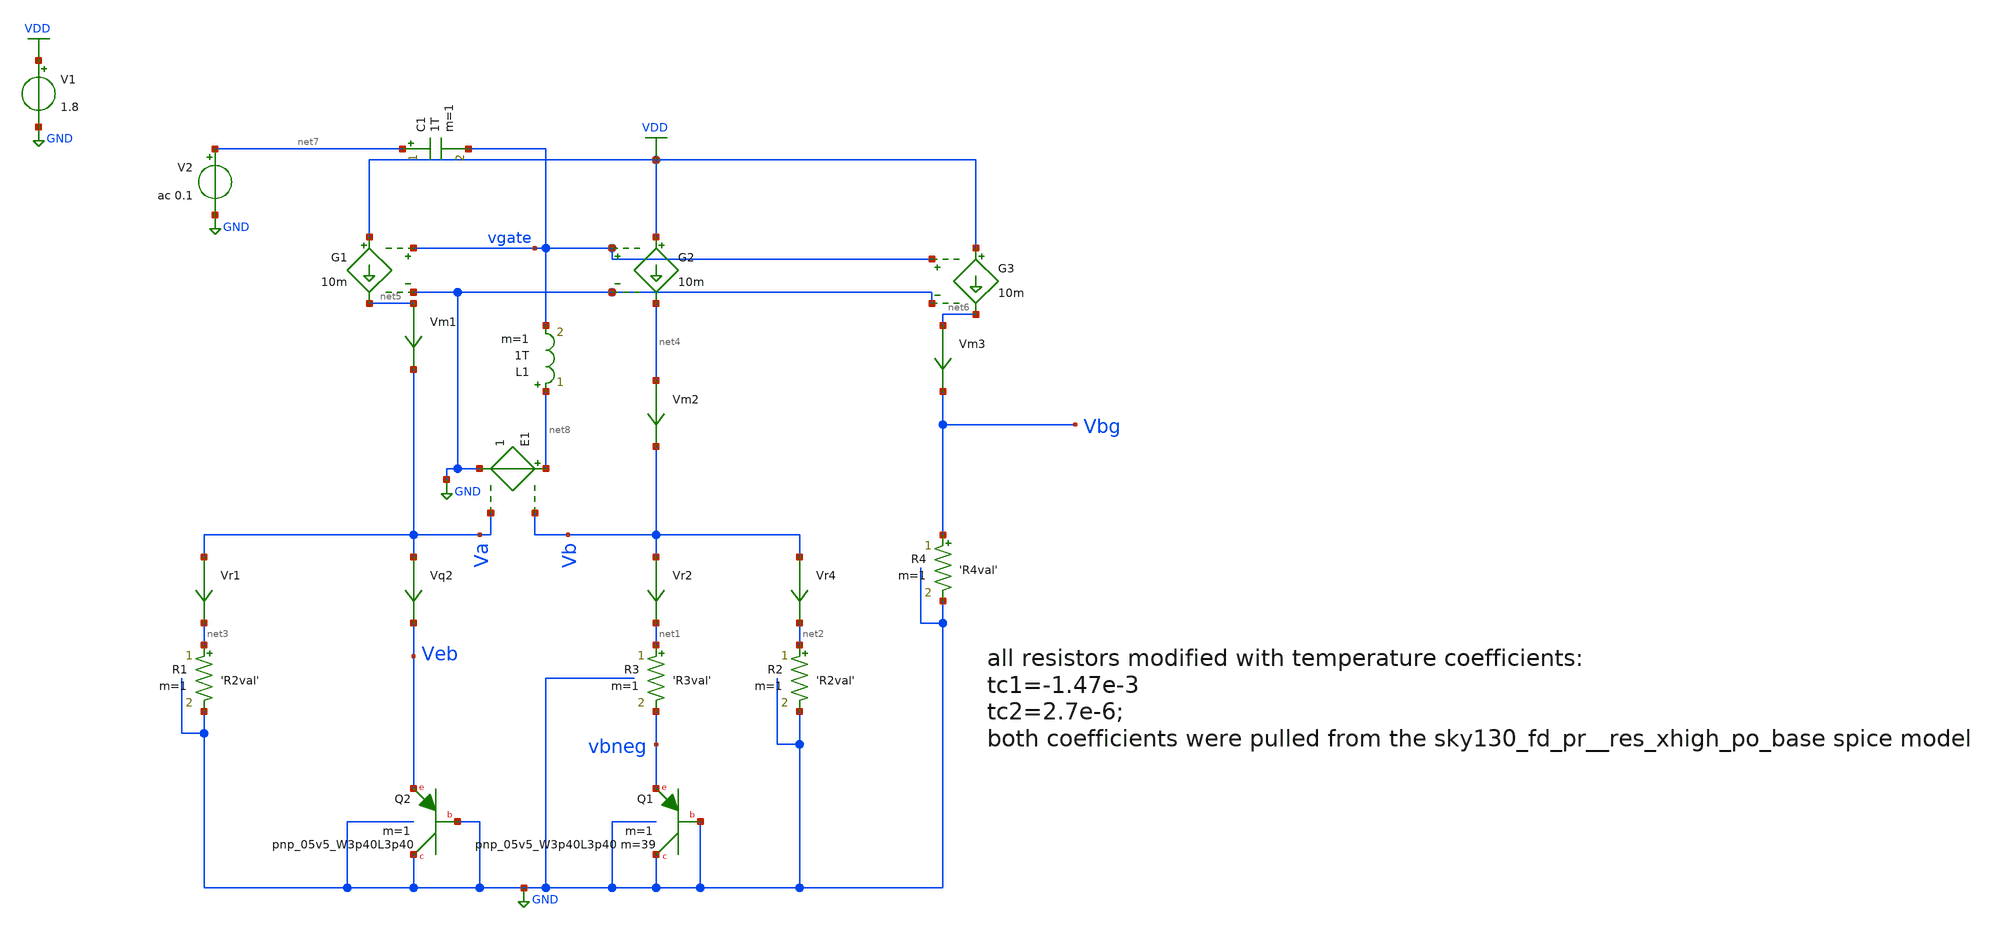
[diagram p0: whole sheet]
** sch_path: schematics/tsmc_bandgap_ideal_feedback.sch
**.subckt tsmc_bandgap_ideal_feedback
XQ2 GND GND Veb sky130_fd_pr__pnp_05v5_W3p40L3p40 m=1
V1 VDD GND 1.8
Vr4 Vb net2 0
.save i(vr4)
Vr2 Vb net1 0
.save i(vr2)
Vm1 net5 Va 0
.save i(vm1)
Vm2 net4 Vb 0
.save i(vm2)
Vm3 net6 Vbg 0
.save i(vm3)
Vr1 Va net3 0
.save i(vr1)
Vq2 Va Veb 0
.save i(vq2)
XQ1 GND GND vbneg sky130_fd_pr__pnp_05v5_W3p40L3p40 m=39 m=1
E1 net8 GND Vb Va 1
R3 net1 vbneg 'R3val' m=1
R4 Vbg GND 'R4val' m=1
R1 net3 GND 'R2val' m=1
R2 net2 GND 'R2val' m=1
G1 VDD net5 vgate GND 10m
L1 net8 vgate 1T m=1
C1 net7 vgate 1T m=1
V2 net7 GND ac 0.1
G2 VDD net4 vgate GND 10m
G3 VDD net6 vgate GND 10m
**** begin user architecture code

.include $::SKYWATER_MODELS/cells/nfet_01v8/sky130_fd_pr__nfet_01v8__tt.corner.spice
.include $::SKYWATER_MODELS/cells/nfet_01v8_lvt/sky130_fd_pr__nfet_01v8_lvt__tt.corner.spice
.include $::SKYWATER_MODELS/cells/pfet_01v8/sky130_fd_pr__pfet_01v8__tt.corner.spice
.include $::SKYWATER_MODELS/cells/nfet_03v3_nvt/sky130_fd_pr__nfet_03v3_nvt__tt.corner.spice
.include $::SKYWATER_MODELS/cells/nfet_05v0_nvt/sky130_fd_pr__nfet_05v0_nvt__tt.corner.spice
.include $::SKYWATER_MODELS/cells/esd_nfet_01v8/sky130_fd_pr__esd_nfet_01v8__tt.corner.spice
.include $::SKYWATER_MODELS/cells/pfet_01v8_lvt/sky130_fd_pr__pfet_01v8_lvt__tt.corner.spice
.include $::SKYWATER_MODELS/cells/pfet_01v8_hvt/sky130_fd_pr__pfet_01v8_hvt__tt.corner.spice
.include $::SKYWATER_MODELS/cells/esd_pfet_g5v0d10v5/sky130_fd_pr__esd_pfet_g5v0d10v5__tt.corner.spice
.include $::SKYWATER_MODELS/cells/pfet_g5v0d10v5/sky130_fd_pr__pfet_g5v0d10v5__tt.corner.spice
.include $::SKYWATER_MODELS/cells/pfet_g5v0d16v0/sky130_fd_pr__pfet_g5v0d16v0__tt.corner.spice
.include $::SKYWATER_MODELS/cells/nfet_g5v0d10v5/sky130_fd_pr__nfet_g5v0d10v5__tt.corner.spice
.include $::SKYWATER_MODELS/cells/nfet_g5v0d16v0/sky130_fd_pr__nfet_g5v0d16v0__tt_discrete.corner.spice
.include $::SKYWATER_MODELS/cells/esd_nfet_g5v0d10v5/sky130_fd_pr__esd_nfet_g5v0d10v5__tt.corner.spice
.include $::SKYWATER_MODELS/models/corners/tt/nonfet.spice
* Mismatch parameters
.include $::SKYWATER_MODELS/cells/nfet_01v8/sky130_fd_pr__nfet_01v8__mismatch.corner.spice
.include $::SKYWATER_MODELS/cells/pfet_01v8/sky130_fd_pr__pfet_01v8__mismatch.corner.spice
.include $::SKYWATER_MODELS/cells/nfet_01v8_lvt/sky130_fd_pr__nfet_01v8_lvt__mismatch.corner.spice
.include $::SKYWATER_MODELS/cells/pfet_01v8_lvt/sky130_fd_pr__pfet_01v8_lvt__mismatch.corner.spice
.include $::SKYWATER_MODELS/cells/pfet_01v8_hvt/sky130_fd_pr__pfet_01v8_hvt__mismatch.corner.spice
.include $::SKYWATER_MODELS/cells/nfet_g5v0d10v5/sky130_fd_pr__nfet_g5v0d10v5__mismatch.corner.spice
.include $::SKYWATER_MODELS/cells/pfet_g5v0d10v5/sky130_fd_pr__pfet_g5v0d10v5__mismatch.corner.spice
.include $::SKYWATER_MODELS/cells/nfet_05v0_nvt/sky130_fd_pr__nfet_05v0_nvt__mismatch.corner.spice
.include $::SKYWATER_MODELS/cells/nfet_03v3_nvt/sky130_fd_pr__nfet_03v3_nvt__mismatch.corner.spice
* Resistor$::SKYWATER_MODELS/Capacitor
.include $::SKYWATER_MODELS/models/r+c/res_typical__cap_typical.spice
.include $::SKYWATER_MODELS/models/r+c/res_typical__cap_typical__lin.spice
* Special cells
.include $::SKYWATER_MODELS/models/corners/tt/specialized_cells.spice
* All models
.include $::SKYWATER_MODELS/models/all.spice
.include $::SKYWATER_MODELS/cells/pnp_05v5/sky130_fd_pr__pnp_05v5_W3p40L3p40.model.spice
* Corner
.include $::SKYWATER_MODELS/models/corners/tt/rf.spice



.option savecurrents
.option warn=1
.param R3val=20k
.param alpha=1.12439
.param R2R3ratio='4.663181043*alpha'
.param R2val='R3val*R2R3ratio'
.param R4R2ratio=0.47924034354
.param R4val='R2val*R4R2ratio'
.control
save all
dc TEMP  -140 140 0.1
plot Vbg
plot deriv(Vbg)
let i = vm3#branch
let indx = 1670
*indx is the index of temperature sweep for 27degC
echo 'Vbg @ 27degC'
let vbg27c = vbg[indx]
print vbg27c
echo 'dVbe/degC & ppm @ 27degC'
print deriv(vbg)[indx] deriv(vbg)[indx]/vbg27c
plot deriv(vbg)/vbg27c
plot v(va, vb) vs i
plot vm1#branch vm2#branch vm3#branch
let vsg = vdd - vgate
let vsd1 = vdd - va
let vsd2 = vdd - vb
let vsd3 = vdd - vbg
let vth = @m.xm1.msky130_fd_pr__pfet_01v8['vth']
let vov = vsg - vth
plot vov vsd1 vsd2 vsd3
let deltav = vb - vbneg
let r4 =vbg/@r4[i]
let r1 =va/@r1[i]
let r2 =vb/@r2[i]
let r3 =deltav/@r3[i]
let vptat =(r2/r3*deltav)
plot veb vptat
plot deriv(veb) deriv(vptat)
let TCratio=deriv(veb)/deriv(vptat)
plot TCratio
plot vb - va
echo 'alpha correction factor'
let alpha=TCratio[670]
print alpha
*let t=-140
*let tstop=140
*foreach t -140 -40 0 27 140
*option temp = $t
*ac dec 100 1 1e9
*let gainva=log10(abs(va/0.1))
*let gainvb=log10(abs(vb/0.1))
*let phaseb=(ph(vb/0.1)*180/pi)
*let phasea=(ph(va/0.1)*180/pi)
*plot gainva gainvb
*plot phasea phaseb
*end
.endc


**** end user architecture code
**.ends
.GLOBAL GND
.GLOBAL VDD
.end
